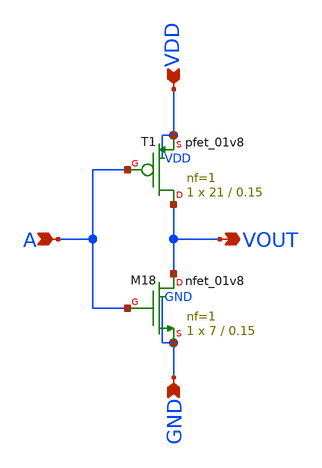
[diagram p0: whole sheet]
** sch_path: CMOS_Inverter_SKY130.sch
**.subckt CMOS_Inverter_SKY130 A VDD GND VOUT
*.ipin A
*.ipin VDD
*.ipin GND
*.opin VOUT
XM18 VOUT A GND GND sky130_fd_pr__nfet_01v8 L=0.15 W=7 nf=1 ad='int((nf+1)/2) * W/nf * 0.29' as='int((nf+2)/2) * W/nf * 0.29'
+ pd='2*int((nf+1)/2) * (W/nf + 0.29)' ps='2*int((nf+2)/2) * (W/nf + 0.29)' nrd='0.29 / W' nrs='0.29 / W'
+ sa=0 sb=0 sd=0 mult=1 m=1
XT1 VOUT A VDD VDD sky130_fd_pr__pfet_01v8 L=0.15 W=21 nf=1 ad='int((1 + 1)/2) * 21 / 1 * 0.29' as='int((1 + 2)/2) * 21 / 1 * 0.29'
+ pd='2*int((1 + 1)/2) * (21 / 1 + 0.29)' ps='2*int((1 + 2)/2) * (21 / 1 + 0.29)' nrd='0.29 / 21 ' nrs='0.29 / 21 '
+ sa=0 sb=0 sd=0 mult=1 m=1
**.ends
.end
